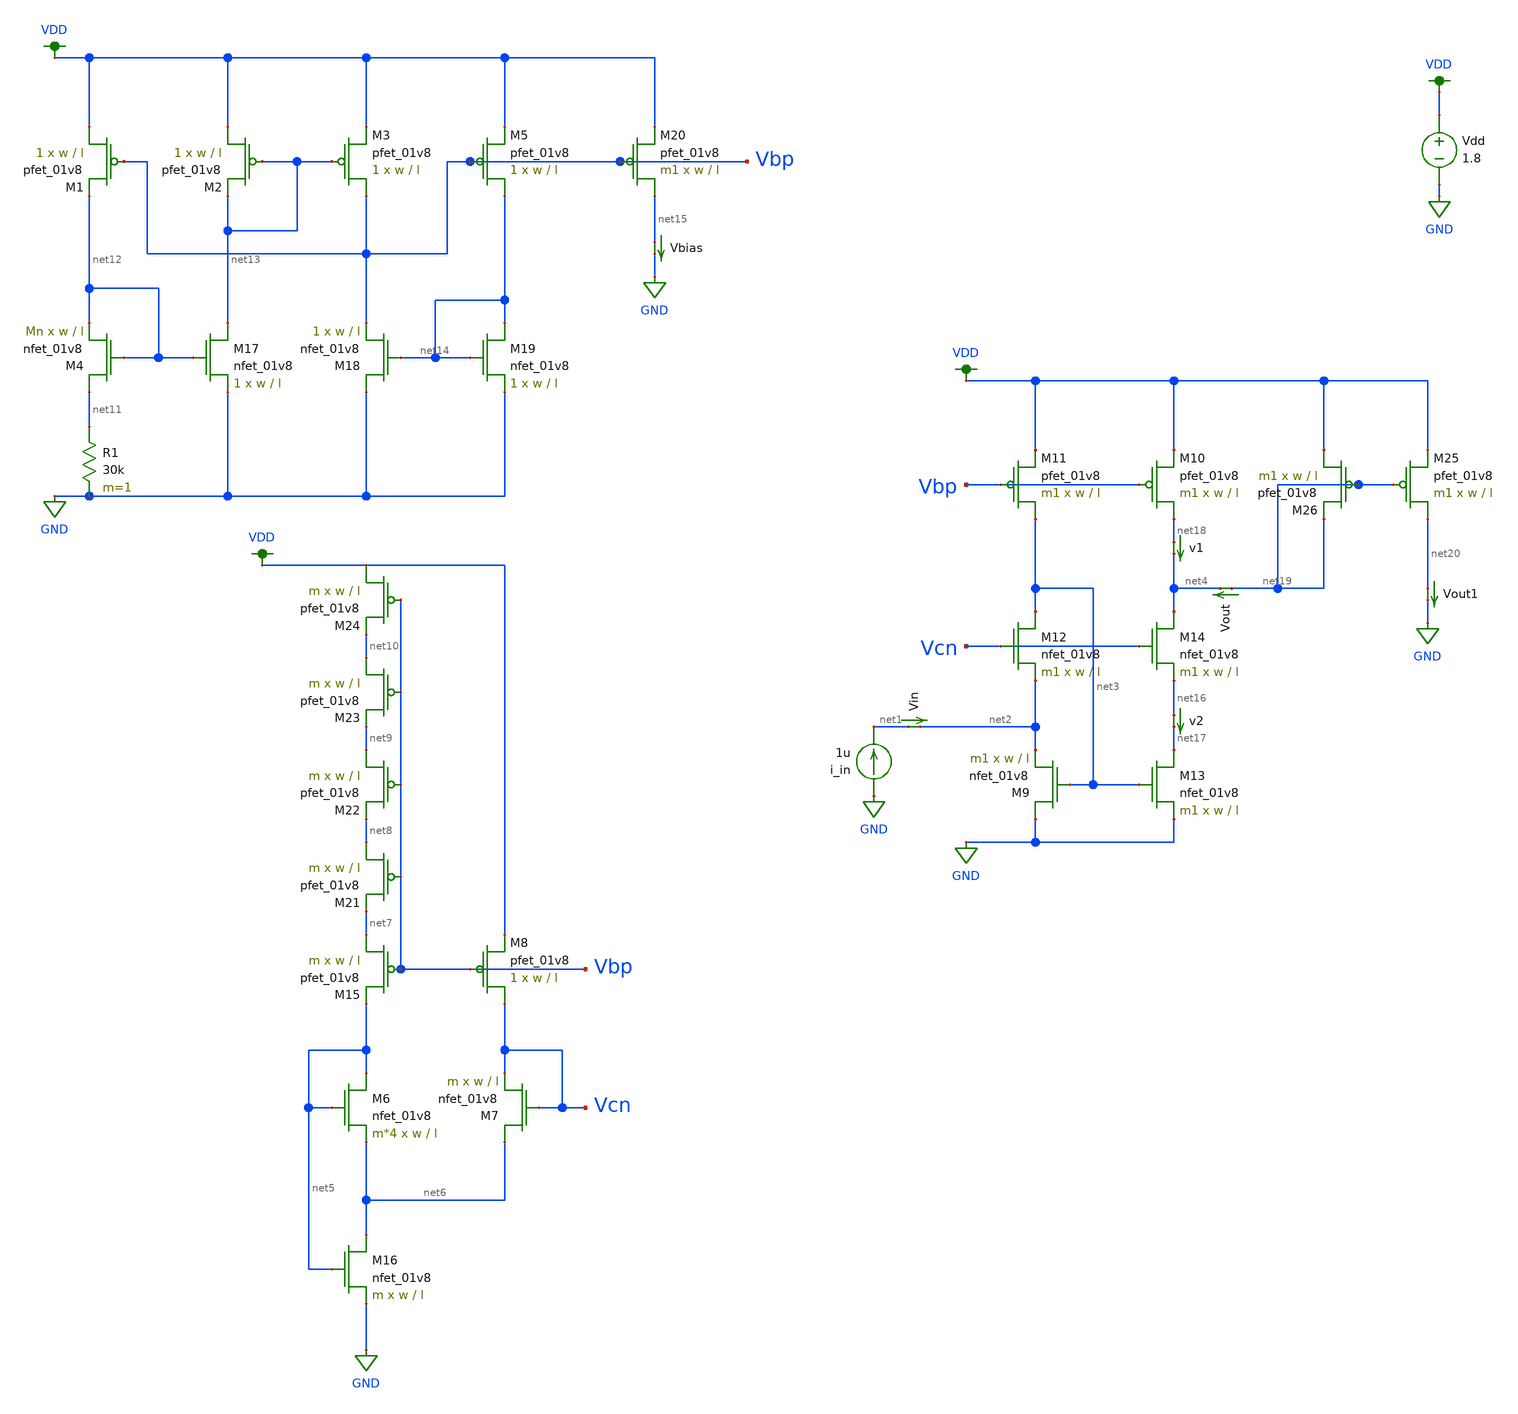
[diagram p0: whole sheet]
** sch_path: schematic/test/iout_mirror.sch
**.subckt iout_mirror
i_in GND net1 1u
Vdd VDD GND 1.8
Vout net19 net4 0
.save i(vout)
Vin net1 net2 0
.save i(vin)
XM10 net18 Vbp VDD VDD sky130_fd_pr__pfet_01v8 L=l W=w nf=1 ad='int((nf+1)/2) * W/nf * 0.29' as='int((nf+2)/2) * W/nf * 0.29'
+ pd='2*int((nf+1)/2) * (W/nf + 0.29)' ps='2*int((nf+2)/2) * (W/nf + 0.29)' nrd='0.29 / W' nrs='0.29 / W'
+ sa=0 sb=0 sd=0 mult=m1 m=m1
XM11 net3 Vbp VDD VDD sky130_fd_pr__pfet_01v8 L=l W=w nf=1 ad='int((nf+1)/2) * W/nf * 0.29' as='int((nf+2)/2) * W/nf * 0.29'
+ pd='2*int((nf+1)/2) * (W/nf + 0.29)' ps='2*int((nf+2)/2) * (W/nf + 0.29)' nrd='0.29 / W' nrs='0.29 / W'
+ sa=0 sb=0 sd=0 mult=m1 m=m1
XM12 net3 Vcn net2 GND sky130_fd_pr__nfet_01v8 L=l W=w nf=1 ad='int((nf+1)/2) * W/nf * 0.29' as='int((nf+2)/2) * W/nf * 0.29'
+ pd='2*int((nf+1)/2) * (W/nf + 0.29)' ps='2*int((nf+2)/2) * (W/nf + 0.29)' nrd='0.29 / W' nrs='0.29 / W'
+ sa=0 sb=0 sd=0 mult=m1 m=m1
XM6 net5 net5 net6 GND sky130_fd_pr__nfet_01v8 L=l W=w nf=1 ad='int((nf+1)/2) * W/nf * 0.29' as='int((nf+2)/2) * W/nf * 0.29'
+ pd='2*int((nf+1)/2) * (W/nf + 0.29)' ps='2*int((nf+2)/2) * (W/nf + 0.29)' nrd='0.29 / W' nrs='0.29 / W'
+ sa=0 sb=0 sd=0 mult=m*4 m=m*4
XM7 net6 Vcn Vcn GND sky130_fd_pr__nfet_01v8 L=l W=w nf=1 ad='int((nf+1)/2) * W/nf * 0.29' as='int((nf+2)/2) * W/nf * 0.29'
+ pd='2*int((nf+1)/2) * (W/nf + 0.29)' ps='2*int((nf+2)/2) * (W/nf + 0.29)' nrd='0.29 / W' nrs='0.29 / W'
+ sa=0 sb=0 sd=0 mult=m m=m
XM8 Vcn Vbp VDD VDD sky130_fd_pr__pfet_01v8 L=l W=w nf=1 ad='int((nf+1)/2) * W/nf * 0.29' as='int((nf+2)/2) * W/nf * 0.29'
+ pd='2*int((nf+1)/2) * (W/nf + 0.29)' ps='2*int((nf+2)/2) * (W/nf + 0.29)' nrd='0.29 / W' nrs='0.29 / W'
+ sa=0 sb=0 sd=0 mult=1 m=1
XM15 net7 Vbp net5 VDD sky130_fd_pr__pfet_01v8 L=l W=w nf=1 ad='int((nf+1)/2) * W/nf * 0.29' as='int((nf+2)/2) * W/nf * 0.29'
+ pd='2*int((nf+1)/2) * (W/nf + 0.29)' ps='2*int((nf+2)/2) * (W/nf + 0.29)' nrd='0.29 / W' nrs='0.29 / W'
+ sa=0 sb=0 sd=0 mult=m m=m
XM16 net6 net5 GND GND sky130_fd_pr__nfet_01v8 L=l W=w nf=1 ad='int((nf+1)/2) * W/nf * 0.29' as='int((nf+2)/2) * W/nf * 0.29'
+ pd='2*int((nf+1)/2) * (W/nf + 0.29)' ps='2*int((nf+2)/2) * (W/nf + 0.29)' nrd='0.29 / W' nrs='0.29 / W'
+ sa=0 sb=0 sd=0 mult=m m=m
XM21 net8 Vbp net7 VDD sky130_fd_pr__pfet_01v8 L=l W=w nf=1 ad='int((nf+1)/2) * W/nf * 0.29' as='int((nf+2)/2) * W/nf * 0.29'
+ pd='2*int((nf+1)/2) * (W/nf + 0.29)' ps='2*int((nf+2)/2) * (W/nf + 0.29)' nrd='0.29 / W' nrs='0.29 / W'
+ sa=0 sb=0 sd=0 mult=m m=m
XM22 net9 Vbp net8 VDD sky130_fd_pr__pfet_01v8 L=l W=w nf=1 ad='int((nf+1)/2) * W/nf * 0.29' as='int((nf+2)/2) * W/nf * 0.29'
+ pd='2*int((nf+1)/2) * (W/nf + 0.29)' ps='2*int((nf+2)/2) * (W/nf + 0.29)' nrd='0.29 / W' nrs='0.29 / W'
+ sa=0 sb=0 sd=0 mult=m m=m
XM23 net10 Vbp net9 VDD sky130_fd_pr__pfet_01v8 L=l W=w nf=1 ad='int((nf+1)/2) * W/nf * 0.29' as='int((nf+2)/2) * W/nf * 0.29'
+ pd='2*int((nf+1)/2) * (W/nf + 0.29)' ps='2*int((nf+2)/2) * (W/nf + 0.29)' nrd='0.29 / W' nrs='0.29 / W'
+ sa=0 sb=0 sd=0 mult=m m=m
XM24 VDD Vbp net10 VDD sky130_fd_pr__pfet_01v8 L=l W=w nf=1 ad='int((nf+1)/2) * W/nf * 0.29' as='int((nf+2)/2) * W/nf * 0.29'
+ pd='2*int((nf+1)/2) * (W/nf + 0.29)' ps='2*int((nf+2)/2) * (W/nf + 0.29)' nrd='0.29 / W' nrs='0.29 / W'
+ sa=0 sb=0 sd=0 mult=m m=m
XM1 VDD Vbp net12 VDD sky130_fd_pr__pfet_01v8 L=l W=w nf=1 ad='int((nf+1)/2) * W/nf * 0.29' as='int((nf+2)/2) * W/nf * 0.29'
+ pd='2*int((nf+1)/2) * (W/nf + 0.29)' ps='2*int((nf+2)/2) * (W/nf + 0.29)' nrd='0.29 / W' nrs='0.29 / W'
+ sa=0 sb=0 sd=0 mult=1 m=1
XM2 VDD net13 net13 VDD sky130_fd_pr__pfet_01v8 L=l W=w nf=1 ad='int((nf+1)/2) * W/nf * 0.29' as='int((nf+2)/2) * W/nf * 0.29'
+ pd='2*int((nf+1)/2) * (W/nf + 0.29)' ps='2*int((nf+2)/2) * (W/nf + 0.29)' nrd='0.29 / W' nrs='0.29 / W'
+ sa=0 sb=0 sd=0 mult=1 m=1
XM3 Vbp net13 VDD VDD sky130_fd_pr__pfet_01v8 L=l W=w nf=1 ad='int((nf+1)/2) * W/nf * 0.29' as='int((nf+2)/2) * W/nf * 0.29'
+ pd='2*int((nf+1)/2) * (W/nf + 0.29)' ps='2*int((nf+2)/2) * (W/nf + 0.29)' nrd='0.29 / W' nrs='0.29 / W'
+ sa=0 sb=0 sd=0 mult=1 m=1
XM5 net14 Vbp VDD VDD sky130_fd_pr__pfet_01v8 L=l W=w nf=1 ad='int((nf+1)/2) * W/nf * 0.29' as='int((nf+2)/2) * W/nf * 0.29'
+ pd='2*int((nf+1)/2) * (W/nf + 0.29)' ps='2*int((nf+2)/2) * (W/nf + 0.29)' nrd='0.29 / W' nrs='0.29 / W'
+ sa=0 sb=0 sd=0 mult=1 m=1
XM4 net11 net12 net12 GND sky130_fd_pr__nfet_01v8 L=l W=w nf=1 ad='int((nf+1)/2) * W/nf * 0.29' as='int((nf+2)/2) * W/nf * 0.29'
+ pd='2*int((nf+1)/2) * (W/nf + 0.29)' ps='2*int((nf+2)/2) * (W/nf + 0.29)' nrd='0.29 / W' nrs='0.29 / W'
+ sa=0 sb=0 sd=0 mult=Mn m=Mn
XM17 net13 net12 GND GND sky130_fd_pr__nfet_01v8 L=l W=w nf=1 ad='int((nf+1)/2) * W/nf * 0.29' as='int((nf+2)/2) * W/nf * 0.29'
+ pd='2*int((nf+1)/2) * (W/nf + 0.29)' ps='2*int((nf+2)/2) * (W/nf + 0.29)' nrd='0.29 / W' nrs='0.29 / W'
+ sa=0 sb=0 sd=0 mult=1 m=1
XM18 GND net14 Vbp GND sky130_fd_pr__nfet_01v8 L=l W=w nf=1 ad='int((nf+1)/2) * W/nf * 0.29' as='int((nf+2)/2) * W/nf * 0.29'
+ pd='2*int((nf+1)/2) * (W/nf + 0.29)' ps='2*int((nf+2)/2) * (W/nf + 0.29)' nrd='0.29 / W' nrs='0.29 / W'
+ sa=0 sb=0 sd=0 mult=1 m=1
XM19 net14 net14 GND GND sky130_fd_pr__nfet_01v8 L=l W=w nf=1 ad='int((nf+1)/2) * W/nf * 0.29' as='int((nf+2)/2) * W/nf * 0.29'
+ pd='2*int((nf+1)/2) * (W/nf + 0.29)' ps='2*int((nf+2)/2) * (W/nf + 0.29)' nrd='0.29 / W' nrs='0.29 / W'
+ sa=0 sb=0 sd=0 mult=1 m=1
R1 net11 GND 30k m=1
XM20 net15 Vbp VDD VDD sky130_fd_pr__pfet_01v8 L=l W=w nf=1 ad='int((nf+1)/2) * W/nf * 0.29' as='int((nf+2)/2) * W/nf * 0.29'
+ pd='2*int((nf+1)/2) * (W/nf + 0.29)' ps='2*int((nf+2)/2) * (W/nf + 0.29)' nrd='0.29 / W' nrs='0.29 / W'
+ sa=0 sb=0 sd=0 mult=m1 m=m1
Vbias net15 GND 0
.save i(vbias)
v2 net16 net17 0
.save i(v2)
v1 net18 net4 0
.save i(v1)
Vout1 net20 GND 0
.save i(vout1)
XM9 GND net3 net2 GND sky130_fd_pr__nfet_01v8 L=l W=w nf=1 ad='int((nf+1)/2) * W/nf * 0.29' as='int((nf+2)/2) * W/nf * 0.29'
+ pd='2*int((nf+1)/2) * (W/nf + 0.29)' ps='2*int((nf+2)/2) * (W/nf + 0.29)' nrd='0.29 / W' nrs='0.29 / W'
+ sa=0 sb=0 sd=0 mult=m1 m=m1
XM13 net17 net3 GND GND sky130_fd_pr__nfet_01v8 L=l W=w nf=1 ad='int((nf+1)/2) * W/nf * 0.29' as='int((nf+2)/2) * W/nf * 0.29'
+ pd='2*int((nf+1)/2) * (W/nf + 0.29)' ps='2*int((nf+2)/2) * (W/nf + 0.29)' nrd='0.29 / W' nrs='0.29 / W'
+ sa=0 sb=0 sd=0 mult=m1 m=m1
XM14 net4 Vcn net16 GND sky130_fd_pr__nfet_01v8 L=l W=w nf=1 ad='int((nf+1)/2) * W/nf * 0.29' as='int((nf+2)/2) * W/nf * 0.29'
+ pd='2*int((nf+1)/2) * (W/nf + 0.29)' ps='2*int((nf+2)/2) * (W/nf + 0.29)' nrd='0.29 / W' nrs='0.29 / W'
+ sa=0 sb=0 sd=0 mult=m1 m=m1
XM25 net20 net19 VDD VDD sky130_fd_pr__pfet_01v8 L=l W=w nf=1 ad='int((nf+1)/2) * W/nf * 0.29' as='int((nf+2)/2) * W/nf * 0.29'
+ pd='2*int((nf+1)/2) * (W/nf + 0.29)' ps='2*int((nf+2)/2) * (W/nf + 0.29)' nrd='0.29 / W' nrs='0.29 / W'
+ sa=0 sb=0 sd=0 mult=m1 m=m1
XM26 VDD net19 net19 VDD sky130_fd_pr__pfet_01v8 L=l W=w nf=1 ad='int((nf+1)/2) * W/nf * 0.29' as='int((nf+2)/2) * W/nf * 0.29'
+ pd='2*int((nf+1)/2) * (W/nf + 0.29)' ps='2*int((nf+2)/2) * (W/nf + 0.29)' nrd='0.29 / W' nrs='0.29 / W'
+ sa=0 sb=0 sd=0 mult=m1 m=m1
**** begin user architecture code



.param m = 1
.param w = 10
.param l = 2
.param Mn = 8
.param m1 = 2

.control
set wr_vecnames
set wr_singlescale
save all
dc i_in 0 7u .001u
wrdata ~/Desktop/madvlsi/madvlsi_proj_5/data/iout_mirror4.txt i(Vin) i(Vout) i(Vbias) i(v1) i(v2)
+ i(Vout1) v(Vbp) v(Vcn)
.endc



.option wnflag=1
.param MC_SWITCH=0.0
.lib ~/skywater/skywater-pdk/libraries/sky130_fd_pr_ngspice/latest/models/sky130.lib.spice tt

**** end user architecture code
**.ends
.GLOBAL GND
.GLOBAL VDD
.end
